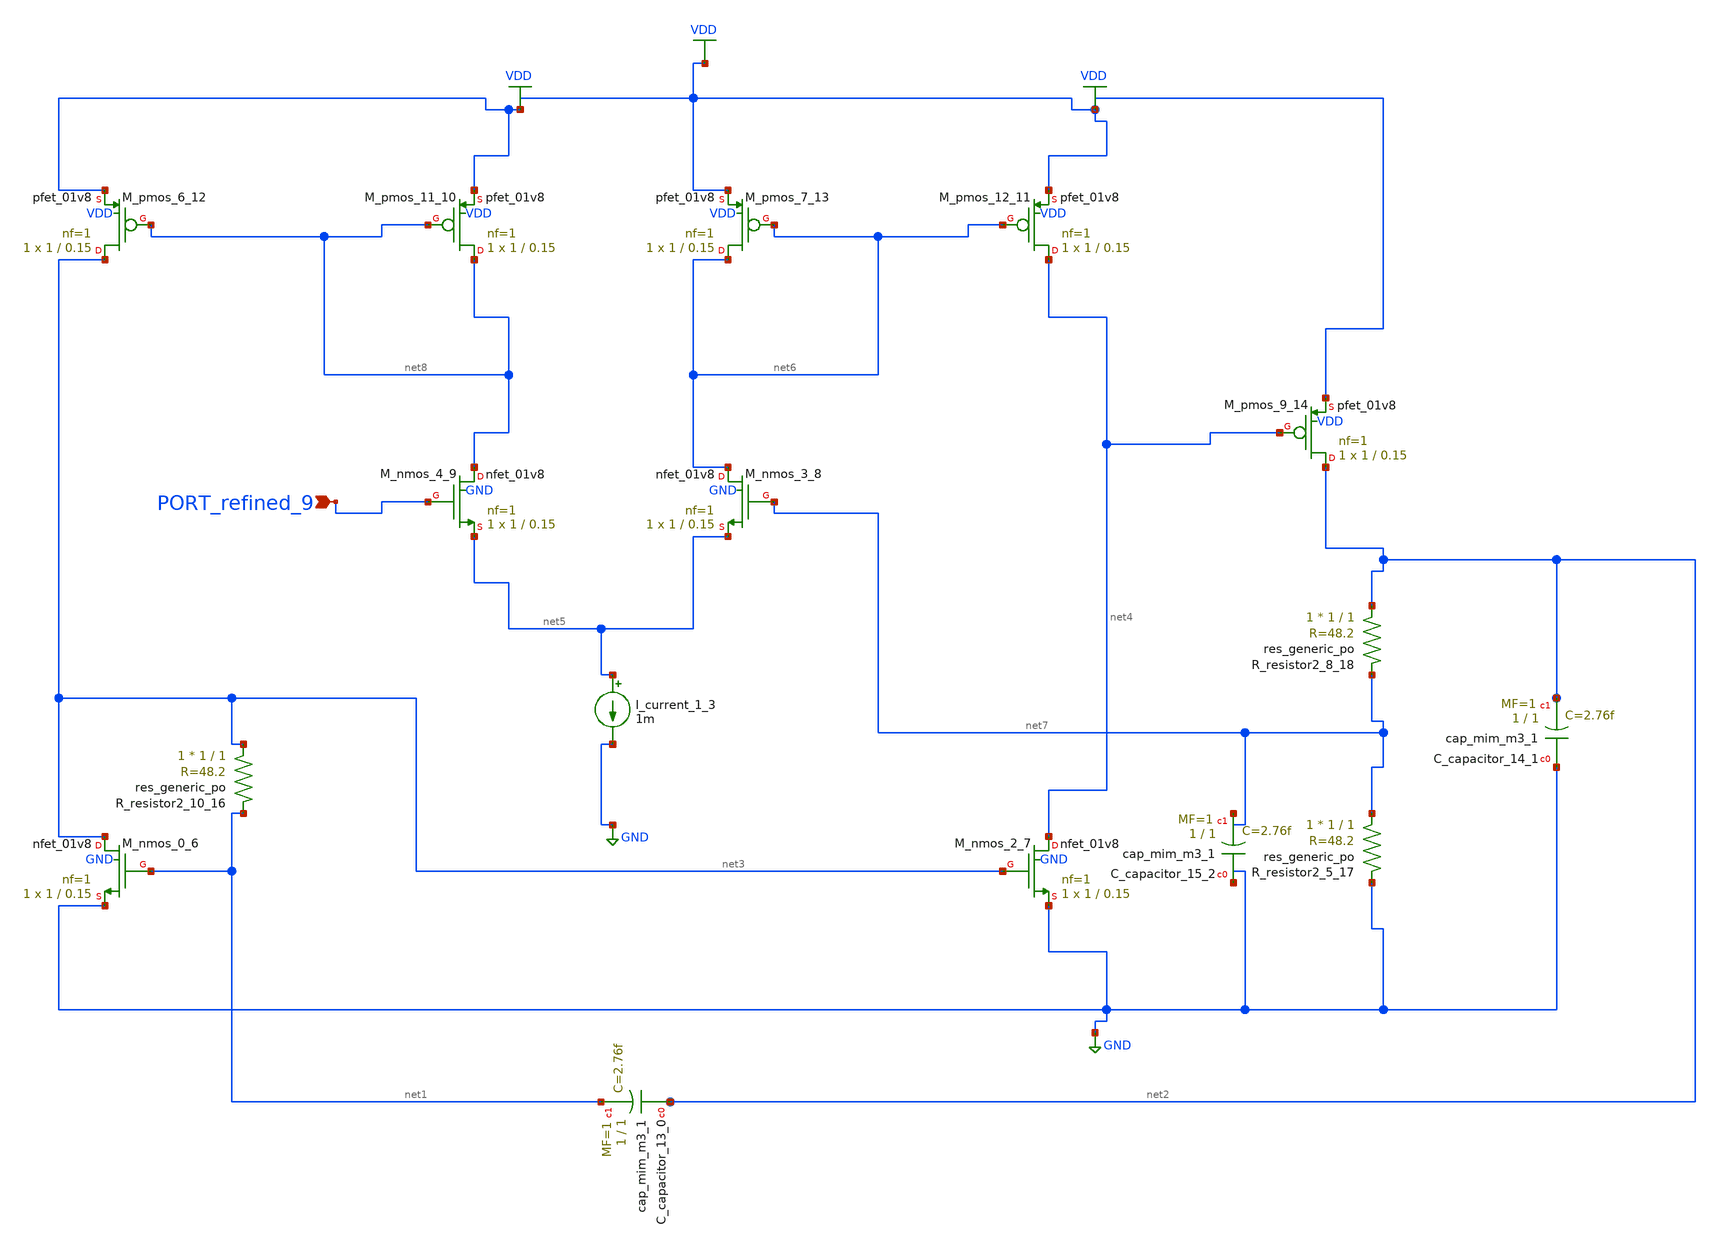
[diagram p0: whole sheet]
** sch_path: schematics/no_doi_01_007.sch
**.subckt no_doi_01_007 PORT_refined_9
*.ipin PORT_refined_9
XC_capacitor_13_0 net2 net1 sky130_fd_pr__cap_mim_m3_1 W=1 L=1 MF=1 m=1
XC_capacitor_14_1 GND net2 sky130_fd_pr__cap_mim_m3_1 W=1 L=1 MF=1 m=1
XC_capacitor_15_2 GND net7 sky130_fd_pr__cap_mim_m3_1 W=1 L=1 MF=1 m=1
I_current_1_3 net5 GND 1m
XM_nmos_0_6 net3 net1 GND GND sky130_fd_pr__nfet_01v8 L=0.15 W=1 nf=1 ad='int((1 + 1)/2) * 1 / 1 * 0.29'
+ as='int((1 + 2)/2) * 1 / 1 * 0.29' pd='2*int((1 + 1)/2) * (1 / 1 + 0.29)' ps='2*int((1 + 2)/2) * (1 / 1 + 0.29)'
+ nrd='0.29 / 1 ' nrs='0.29 / 1 ' sa=0 sb=0 sd=0 mult=1 m=1
XM_nmos_2_7 net4 net3 GND GND sky130_fd_pr__nfet_01v8 L=0.15 W=1 nf=1 ad='int((1 + 1)/2) * 1 / 1 * 0.29'
+ as='int((1 + 2)/2) * 1 / 1 * 0.29' pd='2*int((1 + 1)/2) * (1 / 1 + 0.29)' ps='2*int((1 + 2)/2) * (1 / 1 + 0.29)'
+ nrd='0.29 / 1 ' nrs='0.29 / 1 ' sa=0 sb=0 sd=0 mult=1 m=1
XM_nmos_3_8 net6 net7 net5 GND sky130_fd_pr__nfet_01v8 L=0.15 W=1 nf=1 ad='int((1 + 1)/2) * 1 / 1 * 0.29'
+ as='int((1 + 2)/2) * 1 / 1 * 0.29' pd='2*int((1 + 1)/2) * (1 / 1 + 0.29)' ps='2*int((1 + 2)/2) * (1 / 1 + 0.29)'
+ nrd='0.29 / 1 ' nrs='0.29 / 1 ' sa=0 sb=0 sd=0 mult=1 m=1
XM_nmos_4_9 net8 PORT_refined_9 net5 GND sky130_fd_pr__nfet_01v8 L=0.15 W=1 nf=1 ad='int((1 + 1)/2) * 1 / 1 * 0.29'
+ as='int((1 + 2)/2) * 1 / 1 * 0.29' pd='2*int((1 + 1)/2) * (1 / 1 + 0.29)' ps='2*int((1 + 2)/2) * (1 / 1 + 0.29)'
+ nrd='0.29 / 1 ' nrs='0.29 / 1 ' sa=0 sb=0 sd=0 mult=1 m=1
XM_pmos_11_10 net8 net8 VDD VDD sky130_fd_pr__pfet_01v8 L=0.15 W=1 nf=1 ad='int((1 + 1)/2) * 1 / 1 * 0.29'
+ as='int((1 + 2)/2) * 1 / 1 * 0.29' pd='2*int((1 + 1)/2) * (1 / 1 + 0.29)' ps='2*int((1 + 2)/2) * (1 / 1 + 0.29)'
+ nrd='0.29 / 1 ' nrs='0.29 / 1 ' sa=0 sb=0 sd=0 mult=1 m=1
XM_pmos_12_11 net4 net6 VDD VDD sky130_fd_pr__pfet_01v8 L=0.15 W=1 nf=1 ad='int((1 + 1)/2) * 1 / 1 * 0.29'
+ as='int((1 + 2)/2) * 1 / 1 * 0.29' pd='2*int((1 + 1)/2) * (1 / 1 + 0.29)' ps='2*int((1 + 2)/2) * (1 / 1 + 0.29)'
+ nrd='0.29 / 1 ' nrs='0.29 / 1 ' sa=0 sb=0 sd=0 mult=1 m=1
XM_pmos_6_12 net3 net8 VDD VDD sky130_fd_pr__pfet_01v8 L=0.15 W=1 nf=1 ad='int((1 + 1)/2) * 1 / 1 * 0.29'
+ as='int((1 + 2)/2) * 1 / 1 * 0.29' pd='2*int((1 + 1)/2) * (1 / 1 + 0.29)' ps='2*int((1 + 2)/2) * (1 / 1 + 0.29)'
+ nrd='0.29 / 1 ' nrs='0.29 / 1 ' sa=0 sb=0 sd=0 mult=1 m=1
XM_pmos_7_13 net6 net6 VDD VDD sky130_fd_pr__pfet_01v8 L=0.15 W=1 nf=1 ad='int((1 + 1)/2) * 1 / 1 * 0.29'
+ as='int((1 + 2)/2) * 1 / 1 * 0.29' pd='2*int((1 + 1)/2) * (1 / 1 + 0.29)' ps='2*int((1 + 2)/2) * (1 / 1 + 0.29)'
+ nrd='0.29 / 1 ' nrs='0.29 / 1 ' sa=0 sb=0 sd=0 mult=1 m=1
XM_pmos_9_14 net2 net4 VDD VDD sky130_fd_pr__pfet_01v8 L=0.15 W=1 nf=1 ad='int((1 + 1)/2) * 1 / 1 * 0.29'
+ as='int((1 + 2)/2) * 1 / 1 * 0.29' pd='2*int((1 + 1)/2) * (1 / 1 + 0.29)' ps='2*int((1 + 2)/2) * (1 / 1 + 0.29)'
+ nrd='0.29 / 1 ' nrs='0.29 / 1 ' sa=0 sb=0 sd=0 mult=1 m=1
XR_resistor2_10_16 net3 net1 sky130_fd_pr__res_generic_po W=1 L=1 m=1
XR_resistor2_5_17 net7 GND sky130_fd_pr__res_generic_po W=1 L=1 m=1
XR_resistor2_8_18 net2 net7 sky130_fd_pr__res_generic_po W=1 L=1 m=1
**.ends
.GLOBAL GND
.GLOBAL VDD
.end
